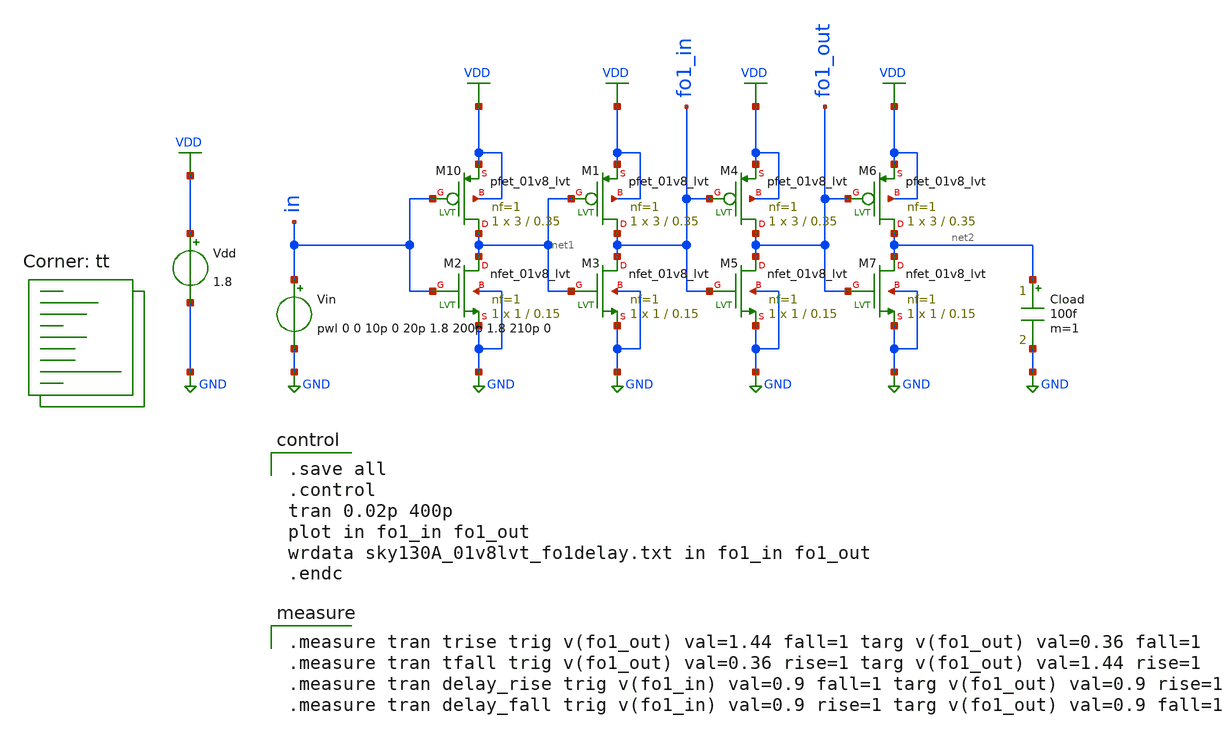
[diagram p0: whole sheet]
** sch_path: xschem/Logic/sky130A_01v8lvt_fo1delay.sch
* Copyright 2021 Stefan Frederik Schippers
* Licensed under the Apache License, Version 2.0 (the "License");
* you may not use this file except in compliance with the License.
* You may obtain a copy of the License at
* https://www.apache.org/licenses/LICENSE-2.0
* Unless required by applicable law or agreed to in writing, software
* distributed under the License is distributed on an "AS IS" BASIS,
* WITHOUT WARRANTIES OR CONDITIONS OF ANY KIND, either express or implied.
* See the License for the specific language governing permissions and
* limitations under the License.
**.subckt sky130A_01v8lvt_fo1delay
Vdd VDD GND 1.8
Vin in GND pwl 0 0 10p 0 20p 1.8 200p 1.8 210p 0
Cload net2 GND 100f m=1
XM10 net1 in VDD VDD sky130_fd_pr__pfet_01v8_lvt L=0.35 W=3 nf=1 ad='int((1 + 1)/2) * 3 / 1 * 0.29' as='int((1 + 2)/2) * 3 / 1 * 0.29'
+ pd='2*int((1 + 1)/2) * (3 / 1 + 0.29)' ps='2*int((1 + 2)/2) * (3 / 1 + 0.29)' nrd='0.29 / 3 ' nrs='0.29 / 3 '
+ sa=0 sb=0 sd=0 mult=1 m=1
XM2 net1 in GND GND sky130_fd_pr__nfet_01v8_lvt L=0.15 W=1 nf=1 ad='int((1 + 1)/2) * 1 / 1 * 0.29' as='int((1 + 2)/2) * 1 / 1 * 0.29'
+ pd='2*int((1 + 1)/2) * (1 / 1 + 0.29)' ps='2*int((1 + 2)/2) * (1 / 1 + 0.29)' nrd='0.29 / 1 ' nrs='0.29 / 1 '
+ sa=0 sb=0 sd=0 mult=1 m=1
XM1 fo1_in net1 VDD VDD sky130_fd_pr__pfet_01v8_lvt L=0.35 W=3 nf=1 ad='int((1 + 1)/2) * 3 / 1 * 0.29'
+ as='int((1 + 2)/2) * 3 / 1 * 0.29' pd='2*int((1 + 1)/2) * (3 / 1 + 0.29)' ps='2*int((1 + 2)/2) * (3 / 1 + 0.29)'
+ nrd='0.29 / 3 ' nrs='0.29 / 3 ' sa=0 sb=0 sd=0 mult=1 m=1
XM3 fo1_in net1 GND GND sky130_fd_pr__nfet_01v8_lvt L=0.15 W=1 nf=1 ad='int((1 + 1)/2) * 1 / 1 * 0.29'
+ as='int((1 + 2)/2) * 1 / 1 * 0.29' pd='2*int((1 + 1)/2) * (1 / 1 + 0.29)' ps='2*int((1 + 2)/2) * (1 / 1 + 0.29)'
+ nrd='0.29 / 1 ' nrs='0.29 / 1 ' sa=0 sb=0 sd=0 mult=1 m=1
XM4 fo1_out fo1_in VDD VDD sky130_fd_pr__pfet_01v8_lvt L=0.35 W=3 nf=1 ad='int((1 + 1)/2) * 3 / 1 * 0.29'
+ as='int((1 + 2)/2) * 3 / 1 * 0.29' pd='2*int((1 + 1)/2) * (3 / 1 + 0.29)' ps='2*int((1 + 2)/2) * (3 / 1 + 0.29)'
+ nrd='0.29 / 3 ' nrs='0.29 / 3 ' sa=0 sb=0 sd=0 mult=1 m=1
XM5 fo1_out fo1_in GND GND sky130_fd_pr__nfet_01v8_lvt L=0.15 W=1 nf=1 ad='int((1 + 1)/2) * 1 / 1 * 0.29'
+ as='int((1 + 2)/2) * 1 / 1 * 0.29' pd='2*int((1 + 1)/2) * (1 / 1 + 0.29)' ps='2*int((1 + 2)/2) * (1 / 1 + 0.29)'
+ nrd='0.29 / 1 ' nrs='0.29 / 1 ' sa=0 sb=0 sd=0 mult=1 m=1
XM6 net2 fo1_out VDD VDD sky130_fd_pr__pfet_01v8_lvt L=0.35 W=3 nf=1 ad='int((1 + 1)/2) * 3 / 1 * 0.29'
+ as='int((1 + 2)/2) * 3 / 1 * 0.29' pd='2*int((1 + 1)/2) * (3 / 1 + 0.29)' ps='2*int((1 + 2)/2) * (3 / 1 + 0.29)'
+ nrd='0.29 / 3 ' nrs='0.29 / 3 ' sa=0 sb=0 sd=0 mult=1 m=1
XM7 net2 fo1_out GND GND sky130_fd_pr__nfet_01v8_lvt L=0.15 W=1 nf=1 ad='int((1 + 1)/2) * 1 / 1 * 0.29'
+ as='int((1 + 2)/2) * 1 / 1 * 0.29' pd='2*int((1 + 1)/2) * (1 / 1 + 0.29)' ps='2*int((1 + 2)/2) * (1 / 1 + 0.29)'
+ nrd='0.29 / 1 ' nrs='0.29 / 1 ' sa=0 sb=0 sd=0 mult=1 m=1
**** begin user architecture code
.lib $::SKYWATER_MODELS/sky130.lib.spice tt

.save all
.control
tran 0.02p 400p
plot in fo1_in fo1_out
wrdata sky130A_01v8lvt_fo1delay.txt in fo1_in fo1_out
.endc


.measure tran trise trig v(fo1_out) val=1.44 fall=1 targ v(fo1_out) val=0.36 fall=1
.measure tran tfall trig v(fo1_out) val=0.36 rise=1 targ v(fo1_out) val=1.44 rise=1
.measure tran delay_rise trig v(fo1_in) val=0.9 fall=1 targ v(fo1_out) val=0.9 rise=1
.measure tran delay_fall trig v(fo1_in) val=0.9 rise=1 targ v(fo1_out) val=0.9 fall=1

**** end user architecture code
**.ends
.GLOBAL VDD
.GLOBAL GND
.end
